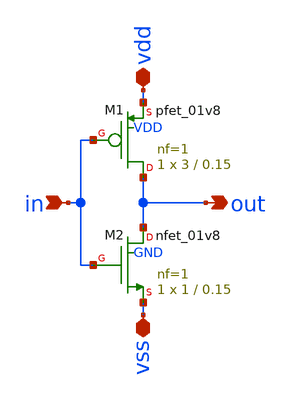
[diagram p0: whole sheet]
** sch_path: samples/cace-tests/inv/xschem/inv.sch
**.subckt inv vdd vss in out
*.iopin vdd
*.iopin vss
*.ipin in
*.opin out
XM1 out in vdd VDD sky130_fd_pr__pfet_01v8 L=0.15 W=3 nf=1 ad='int((nf+1)/2) * W/nf * 0.29' as='int((nf+2)/2) * W/nf * 0.29'
+ pd='2*int((nf+1)/2) * (W/nf + 0.29)' ps='2*int((nf+2)/2) * (W/nf + 0.29)' nrd='0.29 / W' nrs='0.29 / W'
+ sa=0 sb=0 sd=0 mult=1 m=1
XM2 out in vss GND sky130_fd_pr__nfet_01v8 L=0.15 W=1 nf=1 ad='int((nf+1)/2) * W/nf * 0.29' as='int((nf+2)/2) * W/nf * 0.29'
+ pd='2*int((nf+1)/2) * (W/nf + 0.29)' ps='2*int((nf+2)/2) * (W/nf + 0.29)' nrd='0.29 / W' nrs='0.29 / W'
+ sa=0 sb=0 sd=0 mult=1 m=1
**.ends
.end
